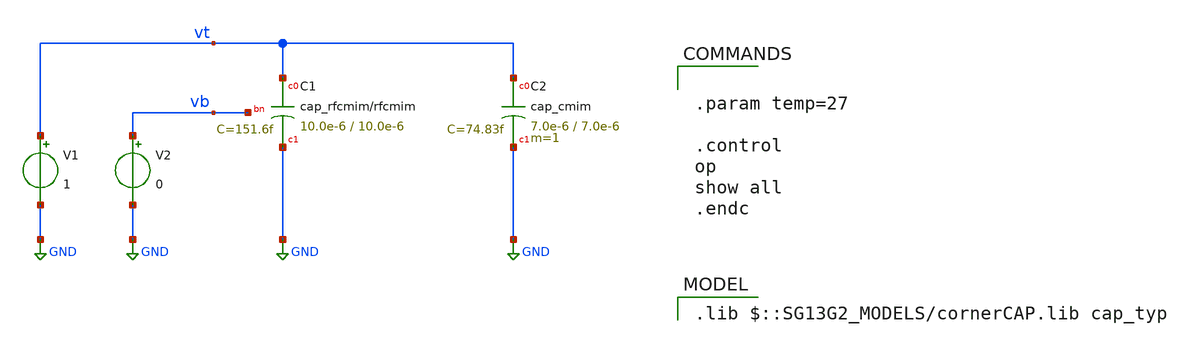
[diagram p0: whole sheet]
** sch_path: 5_Design/3_Real_circuits/sandbox_boris/tb_mimcap.sch
**.subckt tb_mimcap
V1 vt GND 1
XC1 vt GND vb cap_rfcmim w=10.0e-6 l=10.0e-6 wfeed=5.0e-6 m=1 mm_ok=1
XC2 vt GND cap_cmim w=7.0e-6 l=7.0e-6 m=1 mm_ok=1
V2 vb GND 0
**** begin user architecture code
 .lib $::SG13G2_MODELS/cornerCAP.lib cap_typ



.param temp=27

.control
op
show all
.endc


**** end user architecture code
**.ends
.GLOBAL GND
.end
